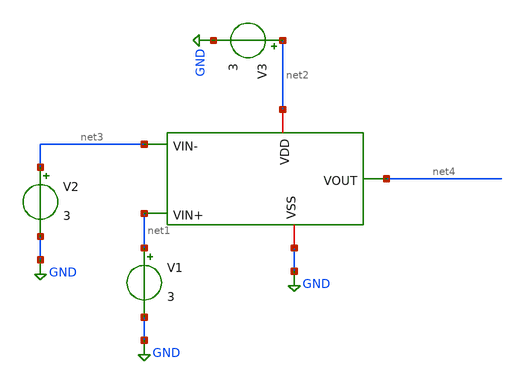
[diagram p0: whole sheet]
** sch_path: xschem/untitled-2.sch
**.subckt untitled-2
x1 net2 net4 net3 net1 GND tso
V1 net1 GND 3
V2 net3 GND 3
V3 net2 GND 3
**.ends

* expanding   symbol:  tso.sym # of pins=5
** sym_path: xschem/tso.sym
** sch_path: xschem/tso.sch
.subckt tso VDD VOUT VIN- VIN+ VSS
*.ipin VIN+
*.opin VOUT
*.iopin VSS
*.iopin VDD
*.ipin VIN-
XM1 net1 VIN- vs1 GND sky130_fd_pr__nfet_01v8 L=0.5 W=2.25 nf=1 ad='int((nf+1)/2) * W/nf * 0.29' as='int((nf+2)/2) * W/nf * 0.29'
+ pd='2*int((nf+1)/2) * (W/nf + 0.29)' ps='2*int((nf+2)/2) * (W/nf + 0.29)' nrd='0.29 / W' nrs='0.29 / W'
+ sa=0 sb=0 sd=0 mult=1 m=1
XM2 vd2 VIN+ vs1 GND sky130_fd_pr__nfet_01v8 L=0.5 W=2.25 nf=1 ad='int((nf+1)/2) * W/nf * 0.29' as='int((nf+2)/2) * W/nf * 0.29'
+ pd='2*int((nf+1)/2) * (W/nf + 0.29)' ps='2*int((nf+2)/2) * (W/nf + 0.29)' nrd='0.29 / W' nrs='0.29 / W'
+ sa=0 sb=0 sd=0 mult=1 m=1
XM3 vd1 vd1 VDD VDD sky130_fd_pr__pfet_01v8 L=0.5 W=15 nf=1 ad='int((nf+1)/2) * W/nf * 0.29' as='int((nf+2)/2) * W/nf * 0.29'
+ pd='2*int((nf+1)/2) * (W/nf + 0.29)' ps='2*int((nf+2)/2) * (W/nf + 0.29)' nrd='0.29 / W' nrs='0.29 / W'
+ sa=0 sb=0 sd=0 mult=1 m=1
XM4 vd2 vd1 VDD VDD sky130_fd_pr__pfet_01v8 L=0.5 W=15 nf=1 ad='int((nf+1)/2) * W/nf * 0.29' as='int((nf+2)/2) * W/nf * 0.29'
+ pd='2*int((nf+1)/2) * (W/nf + 0.29)' ps='2*int((nf+2)/2) * (W/nf + 0.29)' nrd='0.29 / W' nrs='0.29 / W'
+ sa=0 sb=0 sd=0 mult=1 m=1
XM5 net2 vgs5 VSS VSS sky130_fd_pr__nfet_01v8 L=0.5 W=0.75 nf=1 ad='int((nf+1)/2) * W/nf * 0.29' as='int((nf+2)/2) * W/nf * 0.29'
+ pd='2*int((nf+1)/2) * (W/nf + 0.29)' ps='2*int((nf+2)/2) * (W/nf + 0.29)' nrd='0.29 / W' nrs='0.29 / W'
+ sa=0 sb=0 sd=0 mult=1 m=1
XM6 VOUT vd2 VDD VDD sky130_fd_pr__pfet_01v8 L=0.5 W=73 nf=1 ad='int((nf+1)/2) * W/nf * 0.29' as='int((nf+2)/2) * W/nf * 0.29'
+ pd='2*int((nf+1)/2) * (W/nf + 0.29)' ps='2*int((nf+2)/2) * (W/nf + 0.29)' nrd='0.29 / W' nrs='0.29 / W'
+ sa=0 sb=0 sd=0 mult=1 m=1
XM7 VOUT vgs5 VSS VSS sky130_fd_pr__nfet_01v8 L=0.5 W=5.5 nf=1 ad='int((nf+1)/2) * W/nf * 0.29' as='int((nf+2)/2) * W/nf * 0.29'
+ pd='2*int((nf+1)/2) * (W/nf + 0.29)' ps='2*int((nf+2)/2) * (W/nf + 0.29)' nrd='0.29 / W' nrs='0.29 / W'
+ sa=0 sb=0 sd=0 mult=1 m=1
XM8 vgs5 vgs5 VSS VSS sky130_fd_pr__nfet_01v8 L=0.5 W=0.75 nf=1 ad='int((nf+1)/2) * W/nf * 0.29' as='int((nf+2)/2) * W/nf * 0.29'
+ pd='2*int((nf+1)/2) * (W/nf + 0.29)' ps='2*int((nf+2)/2) * (W/nf + 0.29)' nrd='0.29 / W' nrs='0.29 / W'
+ sa=0 sb=0 sd=0 mult=1 m=1
XC1 VOUT vd2 sky130_fd_pr__cap_mim_m3_1 W=25 L=25 MF=4 m=4
XC2 VOUT VSS sky130_fd_pr__cap_mim_m3_1 W=25 L=25 MF=8 m=8
I0 VDD vgs5 0.025m
v5 vd1 net1 0
.save i(v5)
v1 vs1 net2 0
.save i(v1)
.ends

.GLOBAL GND
.end
